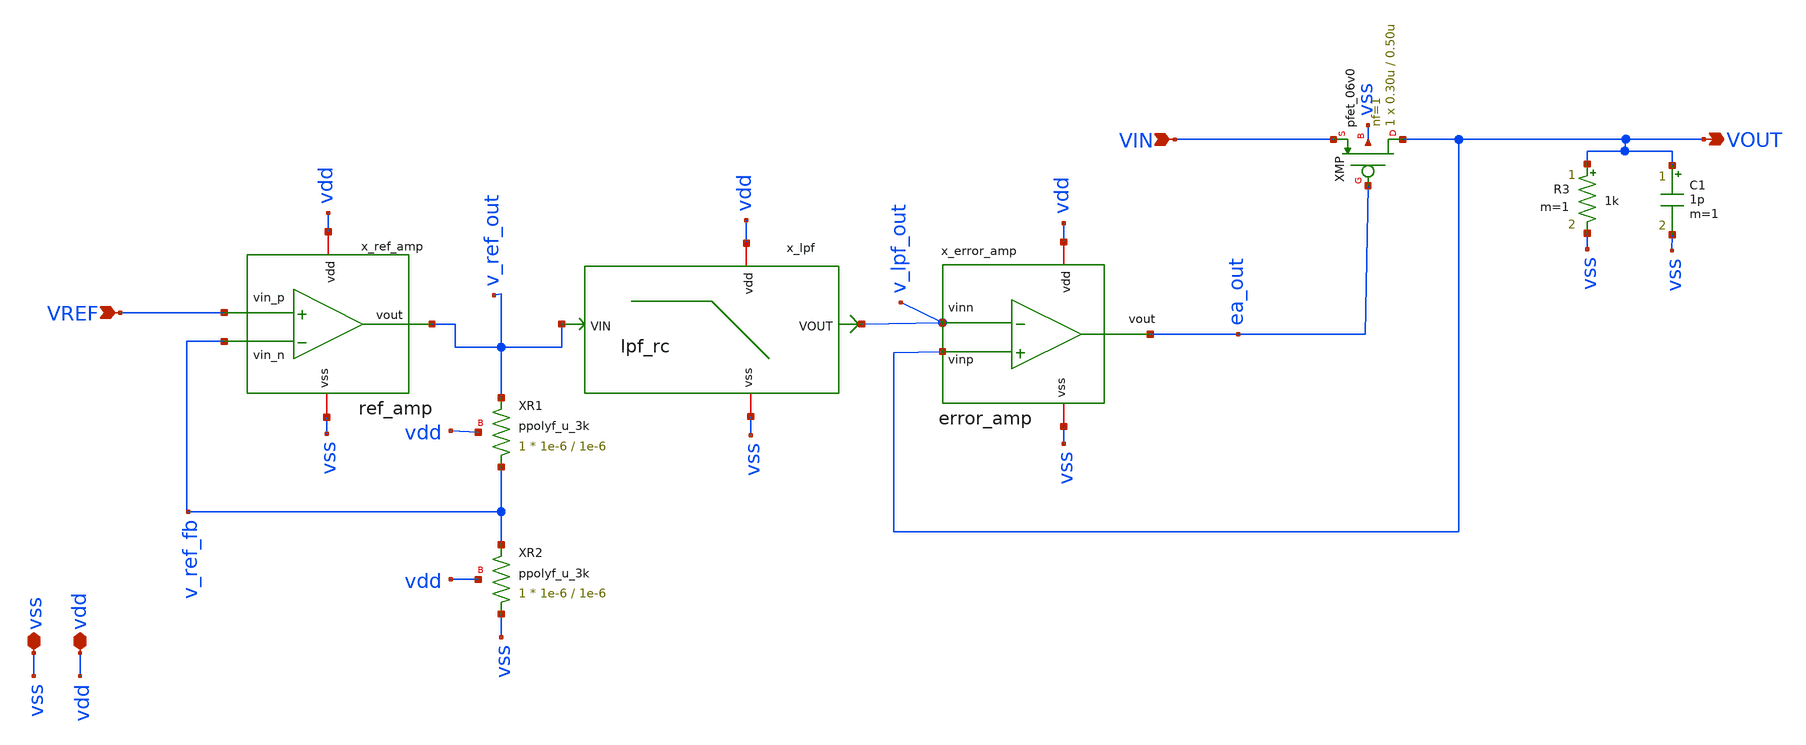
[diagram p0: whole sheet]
** sch_path: analog-db/circuits/ldo_005_buffered_ref/reference/ti-ldo/ldo/ldo_two_r.sch
**.subckt ldo_two_r VREF vdd vss VIN VOUT
*.ipin VREF
*.iopin vdd
*.iopin vss
*.ipin VIN
*.opin VOUT
x_ref_amp VREF v_ref_fb v_ref_out vdd vss ref_amp
XR1 v_ref_fb v_ref_out vdd ppolyf_u_3k r_width=1e-6 r_length=1e-6 m=1
XR2 vss v_ref_fb vdd ppolyf_u_3k r_width=1e-6 r_length=1e-6 m=1
x_error_amp vdd ea_out VOUT v_lpf_out vss error_amp
x_lpf net1 vss v_lpf_out v_ref_out lpf_rc
XMP VOUT ea_out VIN vss pfet_06v0 L=0.50u W=0.30u nf=1 ad='int((nf+1)/2) * W/nf * 0.18u' as='int((nf+2)/2) * W/nf * 0.18u'
+ pd='2*int((nf+1)/2) * (W/nf + 0.18u)' ps='2*int((nf+2)/2) * (W/nf + 0.18u)' nrd='0.18u / W' nrs='0.18u / W'
+ sa=0 sb=0 sd=0 m=1
R3 VOUT vss 1k m=1
C1 VOUT vss 1p m=1
**.ends
.end
